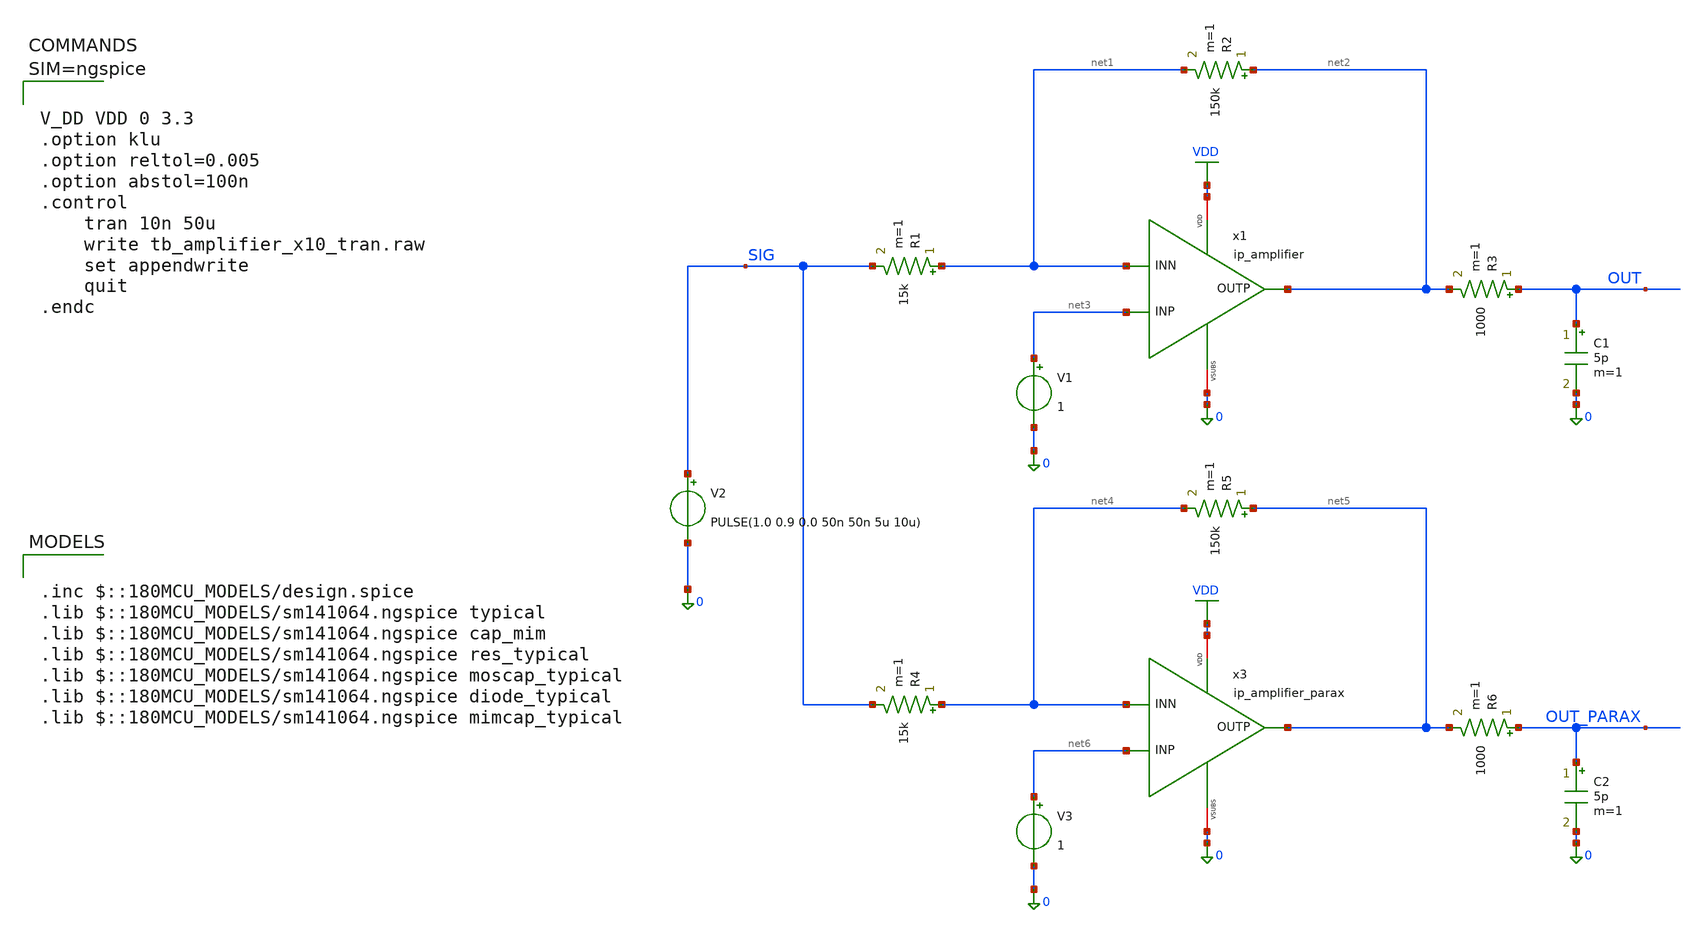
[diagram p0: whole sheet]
** sch_path: analog/xschem/tb_amplifier_x10_tran.sch
**.subckt tb_amplifier_x10_tran
V2 SIG 0 PULSE(1.0 0.9 0.0 50n 50n 5u 10u)
x1 VDD 0 net3 net1 net2 ip_amplifier
R1 net1 SIG 15k m=1
R2 net2 net1 150k m=1
V1 net3 0 1
R3 OUT net2 1000 m=1
C1 OUT 0 5p m=1
R4 net4 SIG 15k m=1
R5 net5 net4 150k m=1
V3 net6 0 1
R6 OUT_PARAX net5 1000 m=1
C2 OUT_PARAX 0 5p m=1
x3 VDD 0 net6 net4 net5 ip_amplifier_parax
**** begin user architecture code

.inc $::180MCU_MODELS/design.spice
.lib $::180MCU_MODELS/sm141064.ngspice typical
.lib $::180MCU_MODELS/sm141064.ngspice cap_mim
.lib $::180MCU_MODELS/sm141064.ngspice res_typical
.lib $::180MCU_MODELS/sm141064.ngspice moscap_typical
.lib $::180MCU_MODELS/sm141064.ngspice diode_typical
.lib $::180MCU_MODELS/sm141064.ngspice mimcap_typical




V_DD VDD 0 3.3
.option klu
.option reltol=0.005
.option abstol=100n
.control
	tran 10n 50u
	write tb_amplifier_x10_tran.raw
	set appendwrite
	quit
.endc



**** end user architecture code
**.ends
.GLOBAL VDD
.end
